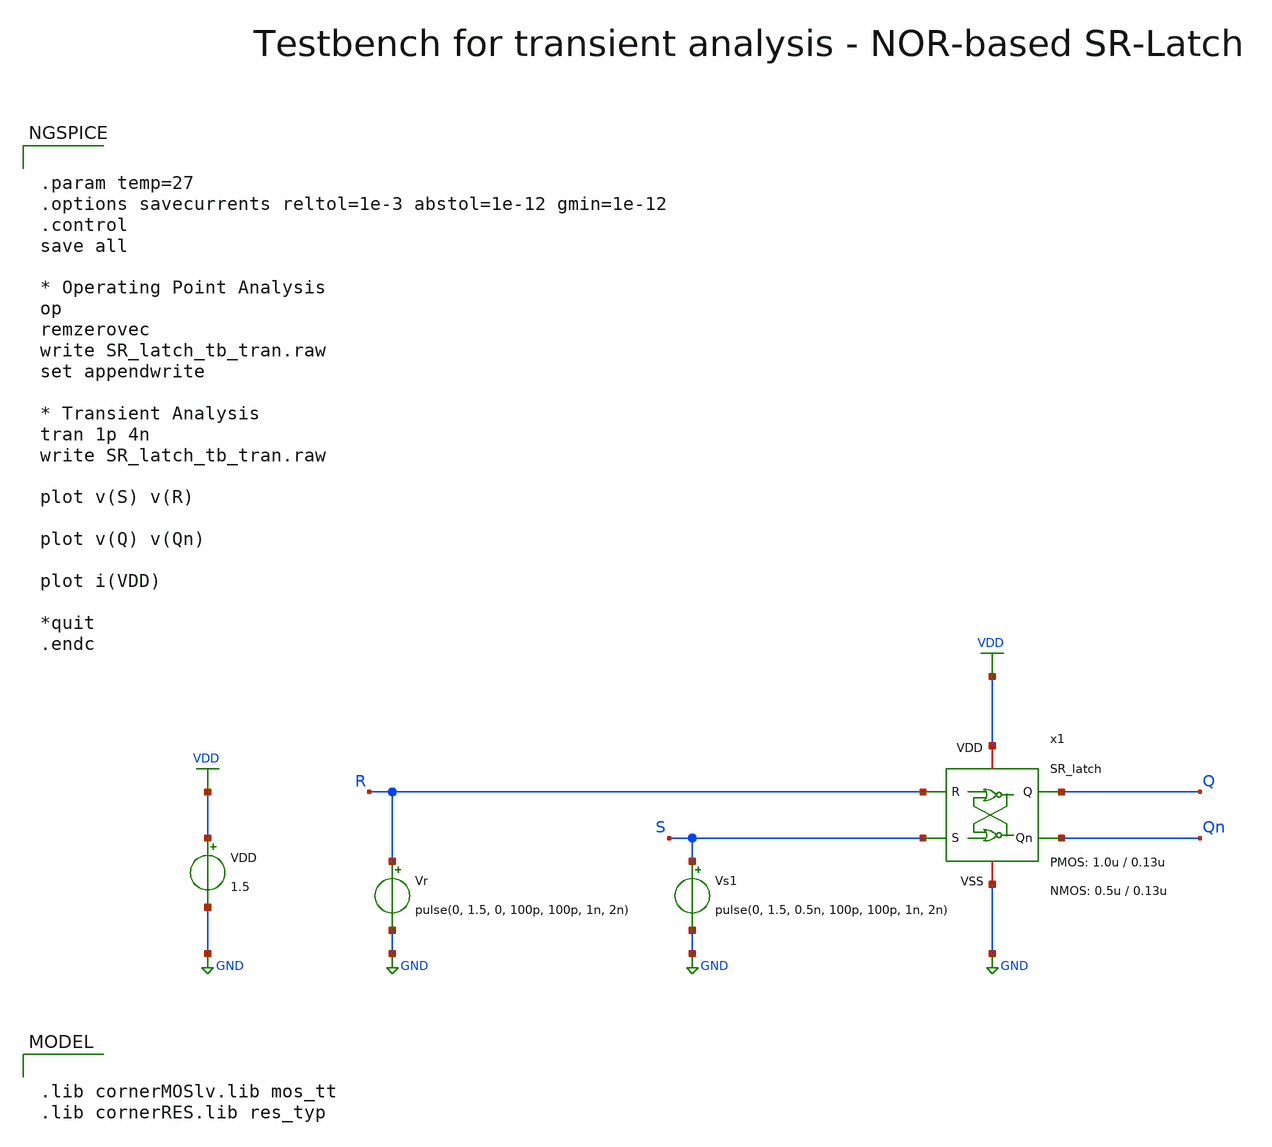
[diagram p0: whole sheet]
** sch_path: SG13G2_ATBS-ADC-main/xschem/comparator/SR_latch/testbenches/SR_latch_tb_tran.sch
**.subckt SR_latch_tb_tran
VDD VDD GND 1.5
Vs1 S GND pulse(0, 1.5, 0.5n, 100p, 100p, 1n, 2n)
Vr R GND pulse(0, 1.5, 0, 100p, 100p, 1n, 2n)
x1 VDD S Qn GND Q R SR_latch W_P_SR=1.0u L_P_SR=0.13u W_N_SR=0.5u L_N_SR=0.13u
**** begin user architecture code

.lib cornerMOSlv.lib mos_tt
.lib cornerRES.lib res_typ



.param temp=27
.options savecurrents reltol=1e-3 abstol=1e-12 gmin=1e-12
.control
save all

* Operating Point Analysis
op
remzerovec
write SR_latch_tb_tran.raw
set appendwrite

* Transient Analysis
tran 1p 4n
write SR_latch_tb_tran.raw

plot v(S) v(R)

plot v(Q) v(Qn)

plot i(VDD)

*quit
.endc

**** end user architecture code
**.ends

* expanding   symbol:  comparator/SR_latch/SR_latch.sym # of pins=6
** sym_path: SG13G2_ATBS-ADC-main/xschem/comparator/SR_latch/SR_latch.sym
** sch_path: SG13G2_ATBS-ADC-main/xschem/comparator/SR_latch/SR_latch.sch
.subckt SR_latch VDD S Qn VSS Q R  W_P_SR=1.0u L_P_SR=0.13u W_N_SR=1.0u L_N_SR=0.13u
*.iopin VDD
*.opin Q
*.iopin VSS
*.ipin S
*.ipin R
*.opin Qn
x1 VDD Q R Qn VSS NOR_gate W_P=W_P_SR L_P=L_P_SR W_N=W_N_SR L_N=L_N_SR
x2 VDD Qn Q S VSS NOR_gate W_P=W_P_SR L_P=L_P_SR W_N=W_N_SR L_N=L_N_SR
.ends


* expanding   symbol:  comparator/NOR_gate/NOR_gate.sym # of pins=5
** sym_path: SG13G2_ATBS-ADC-main/xschem/comparator/NOR_gate/NOR_gate.sym
** sch_path: SG13G2_ATBS-ADC-main/xschem/comparator/NOR_gate/NOR_gate.sch
.subckt NOR_gate VDD C A B VSS  W_P=1.0u L_P=0.13u W_N=0.5u L_N=0.13u
*.iopin VDD
*.opin C
*.iopin VSS
*.ipin A
*.ipin B
XM1 C A VSS VSS sg13_lv_nmos w=W_N l=L_N ng=1 m=1 mm_ok=1
XM2 C B VSS VSS sg13_lv_nmos w=W_N l=L_N ng=1 m=1 mm_ok=1
XM3 C B net1 VDD sg13_lv_pmos w=W_P l=L_P ng=1 m=1 mm_ok=1
XM4 net1 A VDD VDD sg13_lv_pmos w=W_P l=L_P ng=1 m=1 mm_ok=1
XM5 C A net2 VDD sg13_lv_pmos w=W_P l=L_P ng=1 m=1 mm_ok=1
XM6 net2 B VDD VDD sg13_lv_pmos w=W_P l=L_P ng=1 m=1 mm_ok=1
.ends

.GLOBAL GND
.GLOBAL VDD
.end
